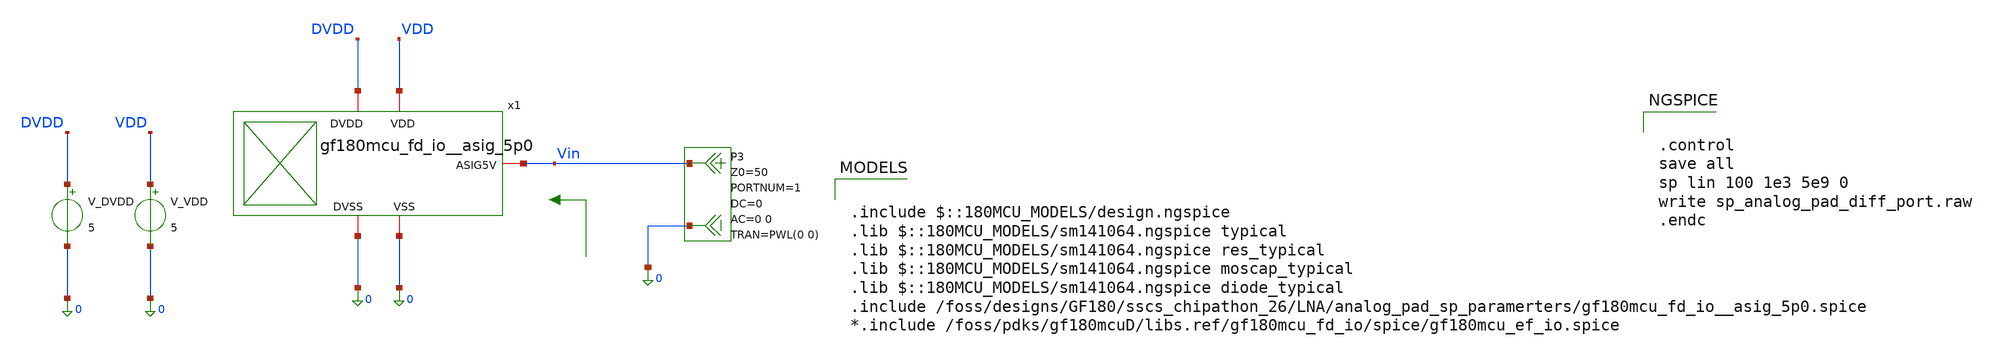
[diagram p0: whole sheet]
** sch_path: analog_pad_sp_paramerters/xschem/schematic_diff_port_sp.sch
**.subckt schematic_diff_port_sp
x1 DVDD Vin 0 VDD 0 gf180mcu_fd_io__asig_5p0
V_VDD VDD 0 5
V_DVDD DVDD 0 5
P3 Vin 0 0 port=1 Z0=50 AC 0 0 PWL(0 0)
**** begin user architecture code


.control
save all
sp lin 100 1e3 5e9 0
write sp_analog_pad_diff_port.raw
.endc



.include $::180MCU_MODELS/design.ngspice
.lib $::180MCU_MODELS/sm141064.ngspice typical
.lib $::180MCU_MODELS/sm141064.ngspice res_typical
.lib $::180MCU_MODELS/sm141064.ngspice moscap_typical
.lib $::180MCU_MODELS/sm141064.ngspice diode_typical
.include /foss/designs/GF180/sscs_chipathon_26/LNA/analog_pad_sp_paramerters/gf180mcu_fd_io__asig_5p0.spice
*.include /foss/pdks/gf180mcuD/libs.ref/gf180mcu_fd_io/spice/gf180mcu_ef_io.spice

**** end user architecture code
**.ends
.end
